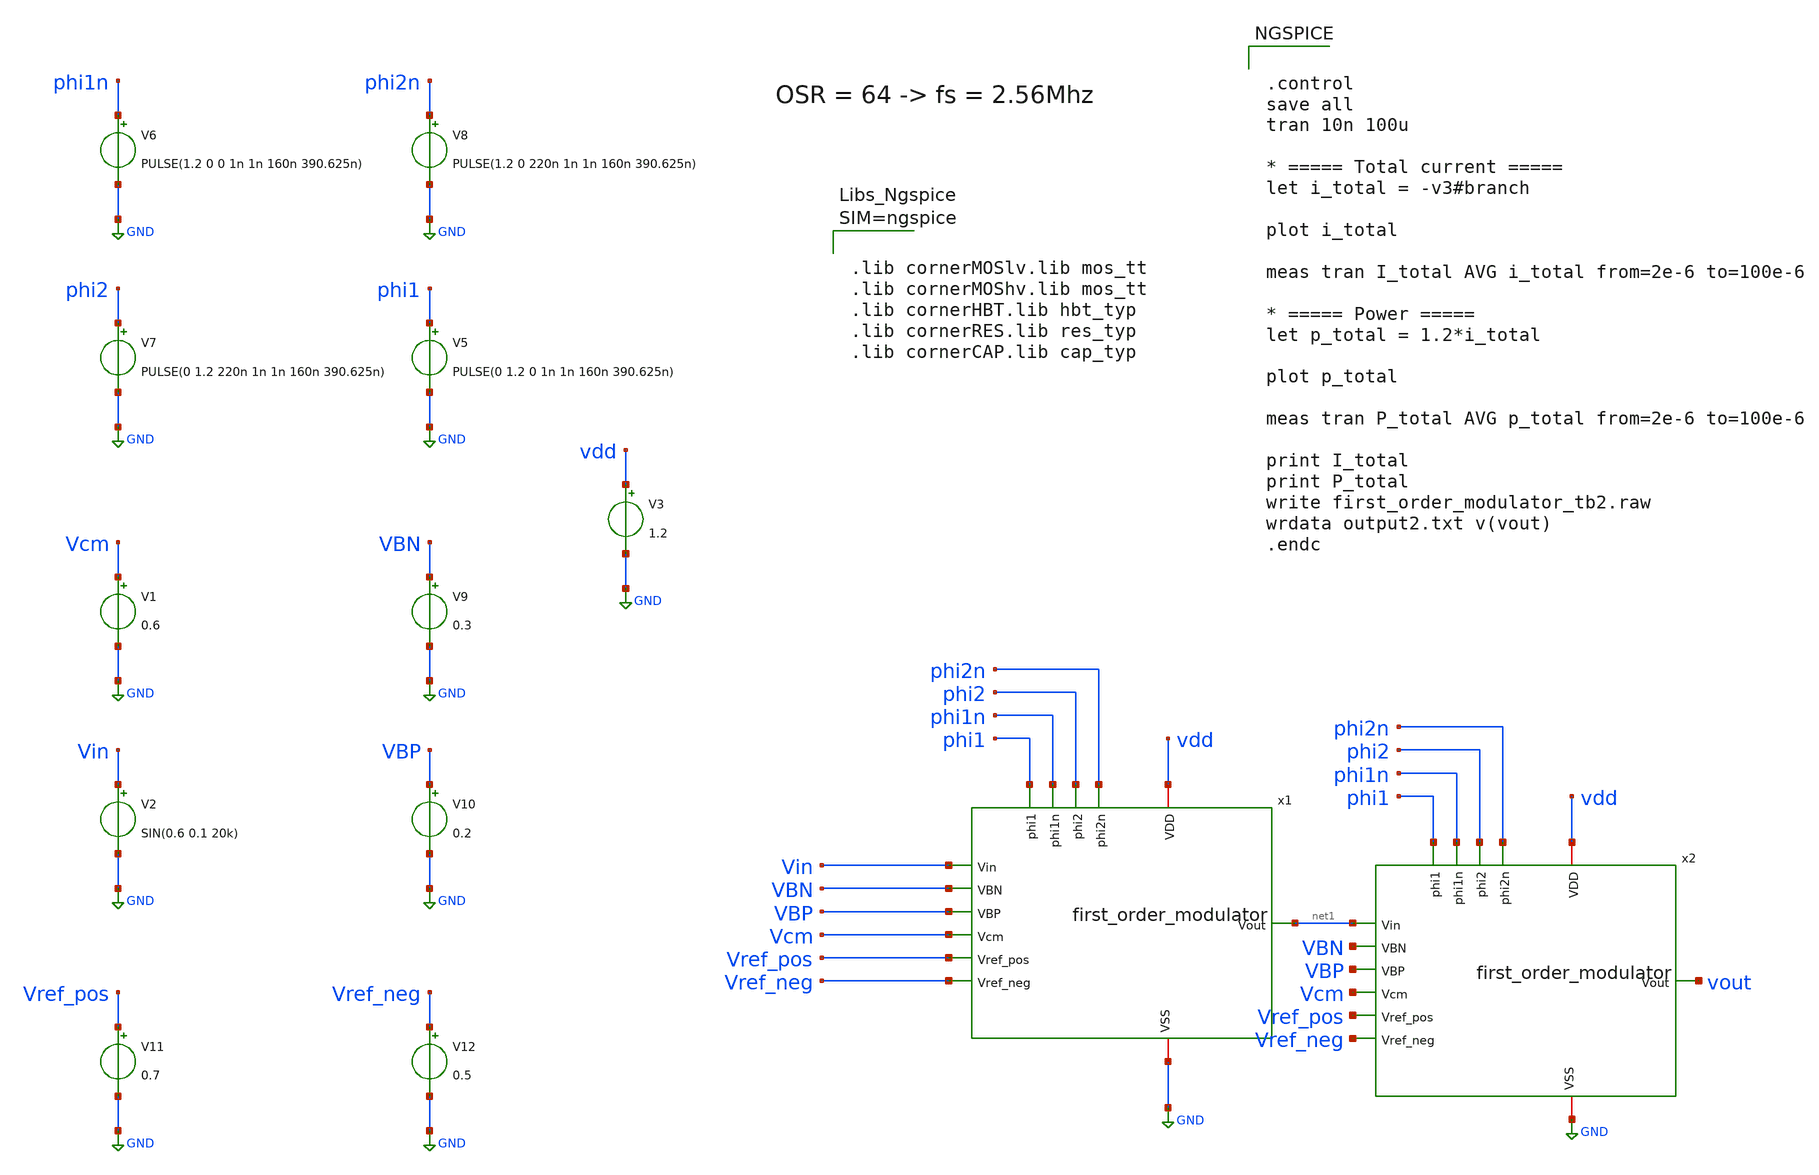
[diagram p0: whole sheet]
** sch_path: xschem/test4.sch
**.subckt test4
V5 phi1 GND PULSE(0 1.2 0 1n 1n 160n 390.625n)
V6 phi1n GND PULSE(1.2 0 0 1n 1n 160n 390.625n)
V7 phi2 GND PULSE(0 1.2 220n 1n 1n 160n 390.625n)
V8 phi2n GND PULSE(1.2 0 220n 1n 1n 160n 390.625n)
V1 Vcm GND 0.6
V2 Vin GND SIN(0.6 0.1 20k)
V3 vdd GND 1.2
V9 VBN GND 0.3
V10 VBP GND 0.2
V12 Vref_neg GND 0.5
V11 Vref_pos GND 0.7
x1 Vin VBN VBP Vcm Vref_pos Vref_neg phi1 phi1n phi2 phi2n vdd GND net1 first_order_modulator
x2 net1 VBN VBP Vcm Vref_pos Vref_neg phi1 phi1n phi2 phi2n vdd GND vout first_order_modulator
**** begin user architecture code


.control
save all
tran 10n 100u

* ===== Total current =====
let i_total = -v3#branch

plot i_total

meas tran I_total AVG i_total from=2e-6 to=100e-6

* ===== Power =====
let p_total = 1.2*i_total

plot p_total

meas tran P_total AVG p_total from=2e-6 to=100e-6

print I_total
print P_total
write first_order_modulator_tb2.raw
wrdata output2.txt v(vout)
.endc





.lib cornerMOSlv.lib mos_tt
.lib cornerMOShv.lib mos_tt
.lib cornerHBT.lib hbt_typ
.lib cornerRES.lib res_typ
.lib cornerCAP.lib cap_typ



**** end user architecture code
**.ends
.GLOBAL GND
.end
